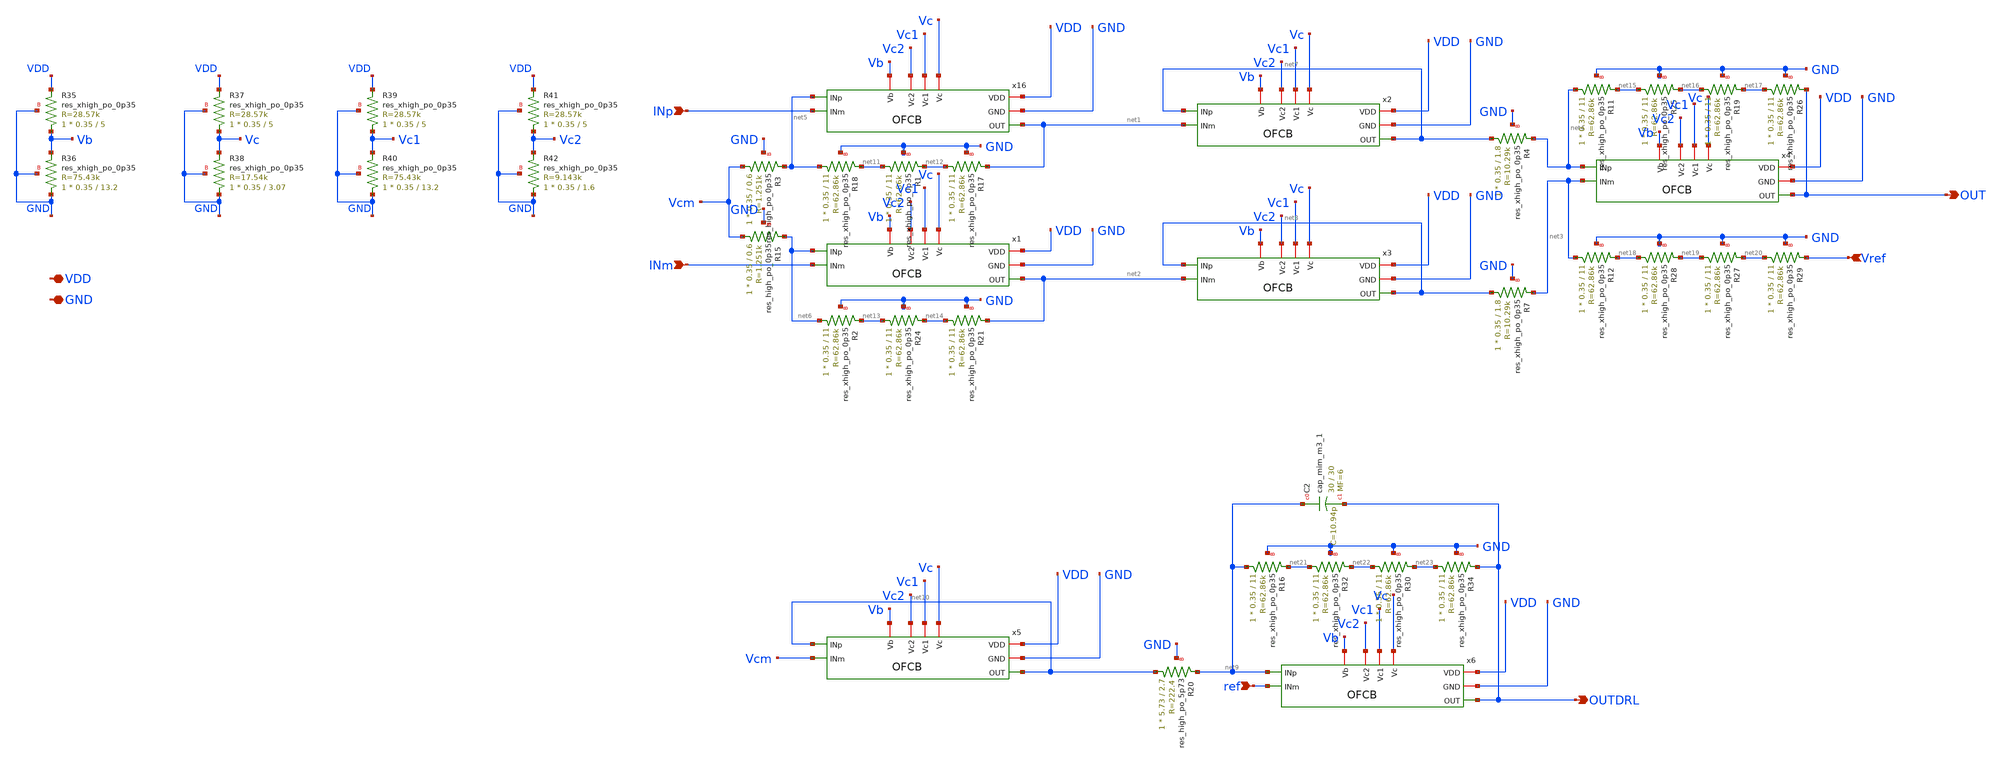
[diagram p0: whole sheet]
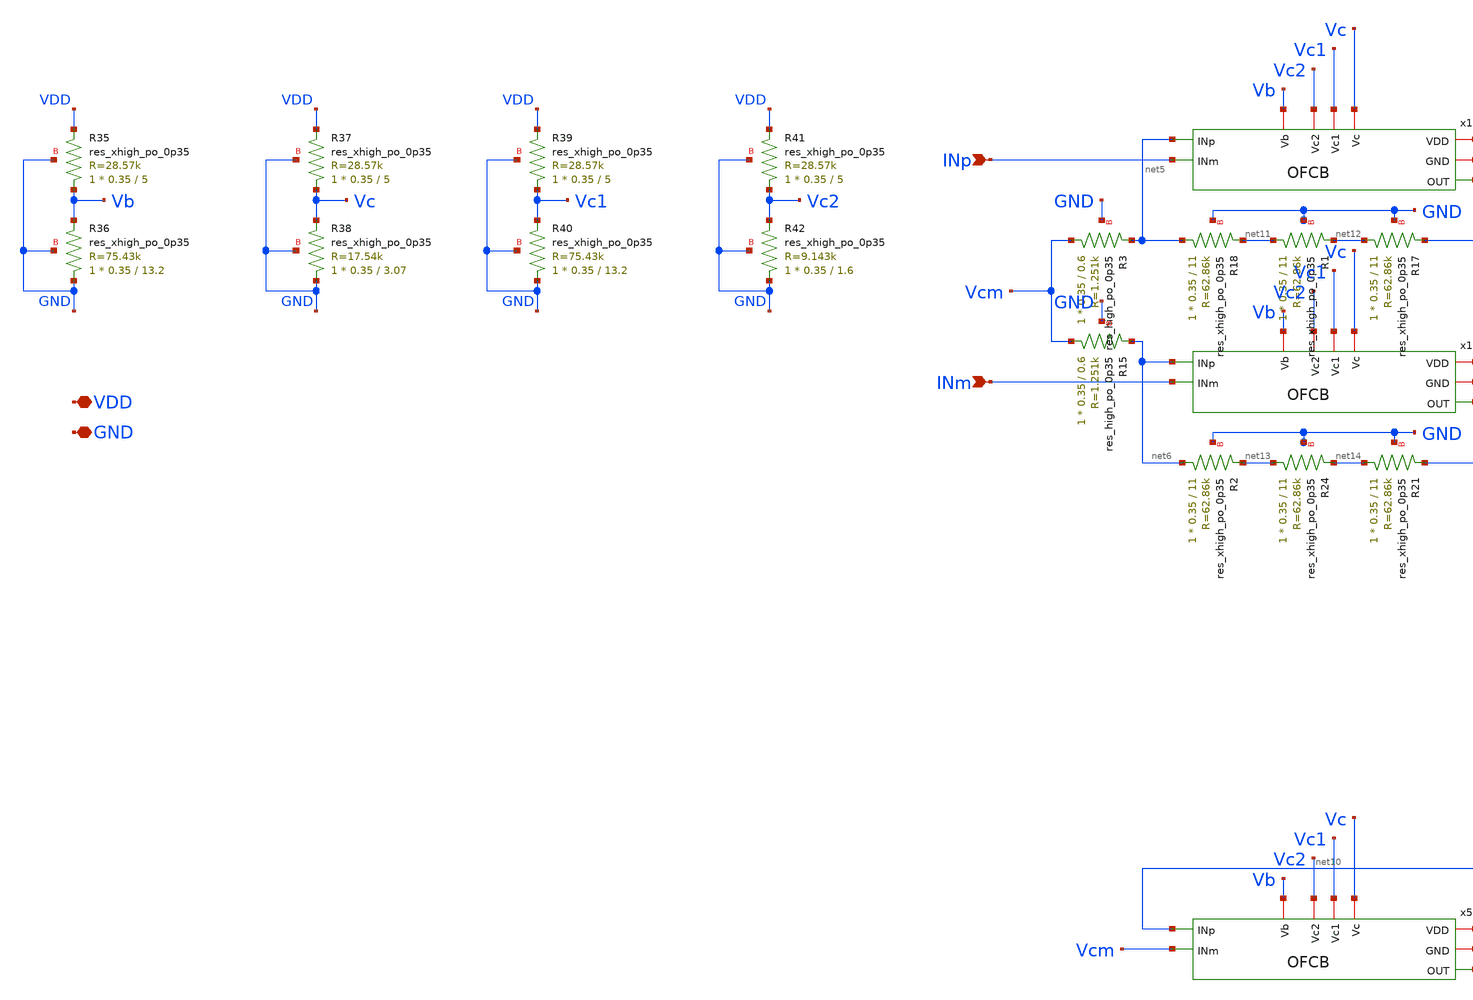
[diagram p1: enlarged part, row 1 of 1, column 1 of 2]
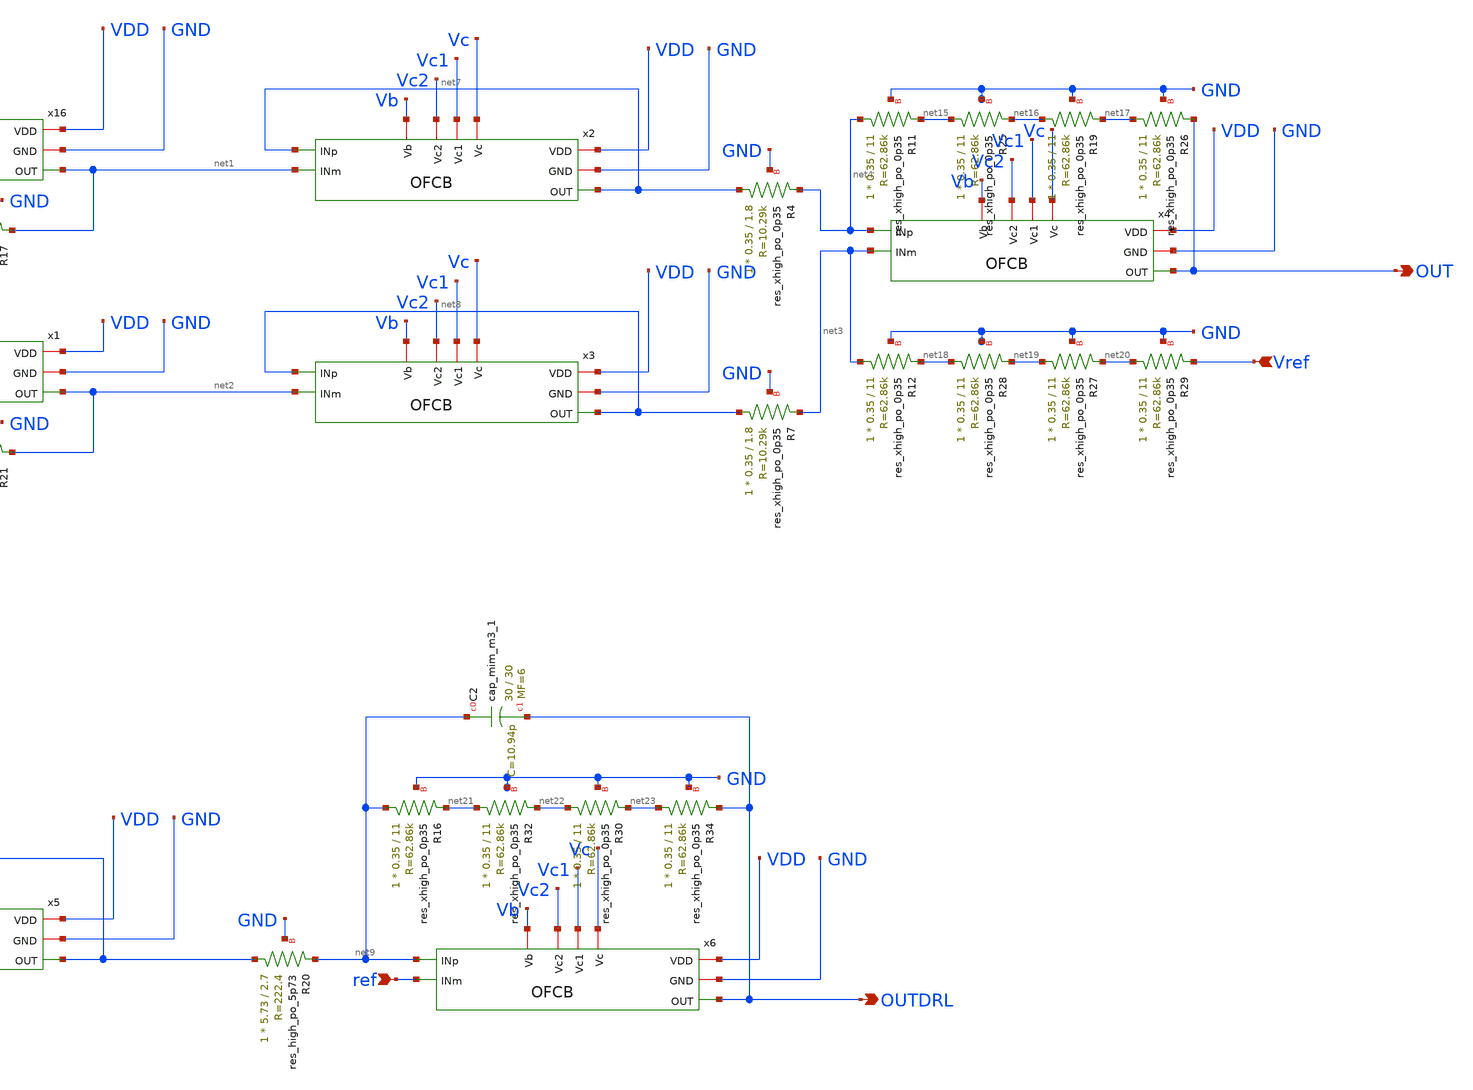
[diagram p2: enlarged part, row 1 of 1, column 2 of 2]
** sch_path: xschem/ecg.sch
**.subckt ecg INp INm OUT Vref OUTDRL ref VDD GND
*.ipin INp
*.ipin INm
*.opin OUT
*.ipin Vref
*.opin OUTDRL
*.ipin ref
*.iopin VDD
*.iopin GND
XR3 Vcm net5 GND sky130_fd_pr__res_high_po_0p35 L=0.6 mult=1 m=1
XR15 Vcm net6 GND sky130_fd_pr__res_high_po_0p35 L=0.6 mult=1 m=1
XR18 net5 net11 GND sky130_fd_pr__res_xhigh_po_0p35 L=11 mult=1 m=1
XR20 net10 net9 GND sky130_fd_pr__res_high_po_5p73 L=2.7 mult=1 m=1
XR17 net12 net1 GND sky130_fd_pr__res_xhigh_po_0p35 L=11 mult=1 m=1
XR1 net11 net12 GND sky130_fd_pr__res_xhigh_po_0p35 L=11 mult=1 m=1
XR2 net6 net13 GND sky130_fd_pr__res_xhigh_po_0p35 L=11 mult=1 m=1
XR21 net14 net2 GND sky130_fd_pr__res_xhigh_po_0p35 L=11 mult=1 m=1
XR24 net13 net14 GND sky130_fd_pr__res_xhigh_po_0p35 L=11 mult=1 m=1
XR4 net7 net4 GND sky130_fd_pr__res_xhigh_po_0p35 L=1.8 mult=1 m=1
XR7 net8 net3 GND sky130_fd_pr__res_xhigh_po_0p35 L=1.8 mult=1 m=1
XR11 net4 net15 GND sky130_fd_pr__res_xhigh_po_0p35 L=11 mult=1 m=1
XR19 net16 net17 GND sky130_fd_pr__res_xhigh_po_0p35 L=11 mult=1 m=1
XR25 net15 net16 GND sky130_fd_pr__res_xhigh_po_0p35 L=11 mult=1 m=1
XR26 net17 OUT GND sky130_fd_pr__res_xhigh_po_0p35 L=11 mult=1 m=1
XR12 net3 net18 GND sky130_fd_pr__res_xhigh_po_0p35 L=11 mult=1 m=1
XR27 net19 net20 GND sky130_fd_pr__res_xhigh_po_0p35 L=11 mult=1 m=1
XR28 net18 net19 GND sky130_fd_pr__res_xhigh_po_0p35 L=11 mult=1 m=1
XR29 net20 Vref GND sky130_fd_pr__res_xhigh_po_0p35 L=11 mult=1 m=1
XC2 net9 OUTDRL sky130_fd_pr__cap_mim_m3_1 W=30 L=30 MF=6 m=6
XR16 net9 net21 GND sky130_fd_pr__res_xhigh_po_0p35 L=11 mult=1 m=1
XR30 net22 net23 GND sky130_fd_pr__res_xhigh_po_0p35 L=11 mult=1 m=1
XR32 net21 net22 GND sky130_fd_pr__res_xhigh_po_0p35 L=11 mult=1 m=1
XR34 net23 OUTDRL GND sky130_fd_pr__res_xhigh_po_0p35 L=11 mult=1 m=1
x16 Vb VDD GND Vc2 net1 net5 INp Vc1 Vc OFCB
x1 Vb VDD GND Vc2 net2 net6 INm Vc1 Vc OFCB
x2 Vb VDD GND Vc2 net7 net7 net1 Vc1 Vc OFCB
x3 Vb VDD GND Vc2 net8 net8 net2 Vc1 Vc OFCB
x4 Vb VDD GND Vc2 OUT net4 net3 Vc1 Vc OFCB
x5 Vb VDD GND Vc2 net10 net10 Vcm Vc1 Vc OFCB
x6 Vb VDD GND Vc2 OUTDRL net9 ref Vc1 Vc OFCB
XR35 Vb VDD GND sky130_fd_pr__res_xhigh_po_0p35 L=5 mult=1 m=1
XR36 GND Vb GND sky130_fd_pr__res_xhigh_po_0p35 L=13.2 mult=1 m=1
XR37 Vc VDD GND sky130_fd_pr__res_xhigh_po_0p35 L=5 mult=1 m=1
XR38 GND Vc GND sky130_fd_pr__res_xhigh_po_0p35 L=3.07 mult=1 m=1
XR39 Vc1 VDD GND sky130_fd_pr__res_xhigh_po_0p35 L=5 mult=1 m=1
XR40 GND Vc1 GND sky130_fd_pr__res_xhigh_po_0p35 L=13.2 mult=1 m=1
XR41 Vc2 VDD GND sky130_fd_pr__res_xhigh_po_0p35 L=5 mult=1 m=1
XR42 GND Vc2 GND sky130_fd_pr__res_xhigh_po_0p35 L=1.6 mult=1 m=1
**.ends

* expanding   symbol:  OFCB.sym # of pins=9
** sym_path: xschem/OFCB.sym
** sch_path: xschem/OFCB.sch
.subckt OFCB Vb VDD GND Vc2 OUT INp INm Vc1 Vc
*.iopin VDD
*.iopin GND
*.opin OUT
*.ipin INp
*.ipin INm
*.iopin Vc2
*.iopin Vc1
*.iopin Vc
*.iopin Vb
XM11 S Vb VDD VDD sky130_fd_pr__pfet_01v8_lvt L=1 W=60 nf=1 ad='int((nf+1)/2) * W/nf * 0.29' as='int((nf+2)/2) * W/nf * 0.29'
+ pd='2*int((nf+1)/2) * (W/nf + 0.29)' ps='2*int((nf+2)/2) * (W/nf + 0.29)' nrd='0.29 / W' nrs='0.29 / W'
+ sa=0 sb=0 sd=0 mult=2 m=2
XM1 D1 INp S S sky130_fd_pr__pfet_01v8_lvt L=10 W=25 nf=2 ad='int((nf+1)/2) * W/nf * 0.29' as='int((nf+2)/2) * W/nf * 0.29'
+ pd='2*int((nf+1)/2) * (W/nf + 0.29)' ps='2*int((nf+2)/2) * (W/nf + 0.29)' nrd='0.29 / W' nrs='0.29 / W'
+ sa=0 sb=0 sd=0 mult=2 m=2
XM2 D2 INm S S sky130_fd_pr__pfet_01v8_lvt L=10 W=25 nf=2 ad='int((nf+1)/2) * W/nf * 0.29' as='int((nf+2)/2) * W/nf * 0.29'
+ pd='2*int((nf+1)/2) * (W/nf + 0.29)' ps='2*int((nf+2)/2) * (W/nf + 0.29)' nrd='0.29 / W' nrs='0.29 / W'
+ sa=0 sb=0 sd=0 mult=2 m=2
XM3 OUT Vc1 D2 GND sky130_fd_pr__nfet_01v8_lvt L=1 W=4 nf=1 ad='int((nf+1)/2) * W/nf * 0.29' as='int((nf+2)/2) * W/nf * 0.29'
+ pd='2*int((nf+1)/2) * (W/nf + 0.29)' ps='2*int((nf+2)/2) * (W/nf + 0.29)' nrd='0.29 / W' nrs='0.29 / W'
+ sa=0 sb=0 sd=0 mult=1 m=1
XM4 D2 Vc GND GND sky130_fd_pr__nfet_01v8_lvt L=1 W=2.8 nf=1 ad='int((nf+1)/2) * W/nf * 0.29' as='int((nf+2)/2) * W/nf * 0.29'
+ pd='2*int((nf+1)/2) * (W/nf + 0.29)' ps='2*int((nf+2)/2) * (W/nf + 0.29)' nrd='0.29 / W' nrs='0.29 / W'
+ sa=0 sb=0 sd=0 mult=1 m=1
XM5 D1 Vc GND GND sky130_fd_pr__nfet_01v8_lvt L=1 W=2.8 nf=1 ad='int((nf+1)/2) * W/nf * 0.29' as='int((nf+2)/2) * W/nf * 0.29'
+ pd='2*int((nf+1)/2) * (W/nf + 0.29)' ps='2*int((nf+2)/2) * (W/nf + 0.29)' nrd='0.29 / W' nrs='0.29 / W'
+ sa=0 sb=0 sd=0 mult=1 m=1
XM6 G Vc1 D1 GND sky130_fd_pr__nfet_01v8_lvt L=1 W=4 nf=1 ad='int((nf+1)/2) * W/nf * 0.29' as='int((nf+2)/2) * W/nf * 0.29'
+ pd='2*int((nf+1)/2) * (W/nf + 0.29)' ps='2*int((nf+2)/2) * (W/nf + 0.29)' nrd='0.29 / W' nrs='0.29 / W'
+ sa=0 sb=0 sd=0 mult=1 m=1
XM7 G Vc2 D9 D9 sky130_fd_pr__pfet_01v8_lvt L=2.23 W=5 nf=1 ad='int((nf+1)/2) * W/nf * 0.29' as='int((nf+2)/2) * W/nf * 0.29'
+ pd='2*int((nf+1)/2) * (W/nf + 0.29)' ps='2*int((nf+2)/2) * (W/nf + 0.29)' nrd='0.29 / W' nrs='0.29 / W'
+ sa=0 sb=0 sd=0 mult=1 m=1
XM9 D9 G VDD VDD sky130_fd_pr__pfet_01v8_lvt L=2.23 W=3.8 nf=1 ad='int((nf+1)/2) * W/nf * 0.29' as='int((nf+2)/2) * W/nf * 0.29'
+ pd='2*int((nf+1)/2) * (W/nf + 0.29)' ps='2*int((nf+2)/2) * (W/nf + 0.29)' nrd='0.29 / W' nrs='0.29 / W'
+ sa=0 sb=0 sd=0 mult=1 m=1
XM8 D10 G VDD VDD sky130_fd_pr__pfet_01v8_lvt L=2.23 W=3.8 nf=1 ad='int((nf+1)/2) * W/nf * 0.29' as='int((nf+2)/2) * W/nf * 0.29'
+ pd='2*int((nf+1)/2) * (W/nf + 0.29)' ps='2*int((nf+2)/2) * (W/nf + 0.29)' nrd='0.29 / W' nrs='0.29 / W'
+ sa=0 sb=0 sd=0 mult=1 m=1
XM10 OUT Vc2 D10 D10 sky130_fd_pr__pfet_01v8_lvt L=2.23 W=5 nf=1 ad='int((nf+1)/2) * W/nf * 0.29' as='int((nf+2)/2) * W/nf * 0.29'
+ pd='2*int((nf+1)/2) * (W/nf + 0.29)' ps='2*int((nf+2)/2) * (W/nf + 0.29)' nrd='0.29 / W' nrs='0.29 / W'
+ sa=0 sb=0 sd=0 mult=1 m=1
XC1 OUT D1 sky130_fd_pr__cap_mim_m3_1 W=50 L=20 MF=1 m=1
.ends

.end
